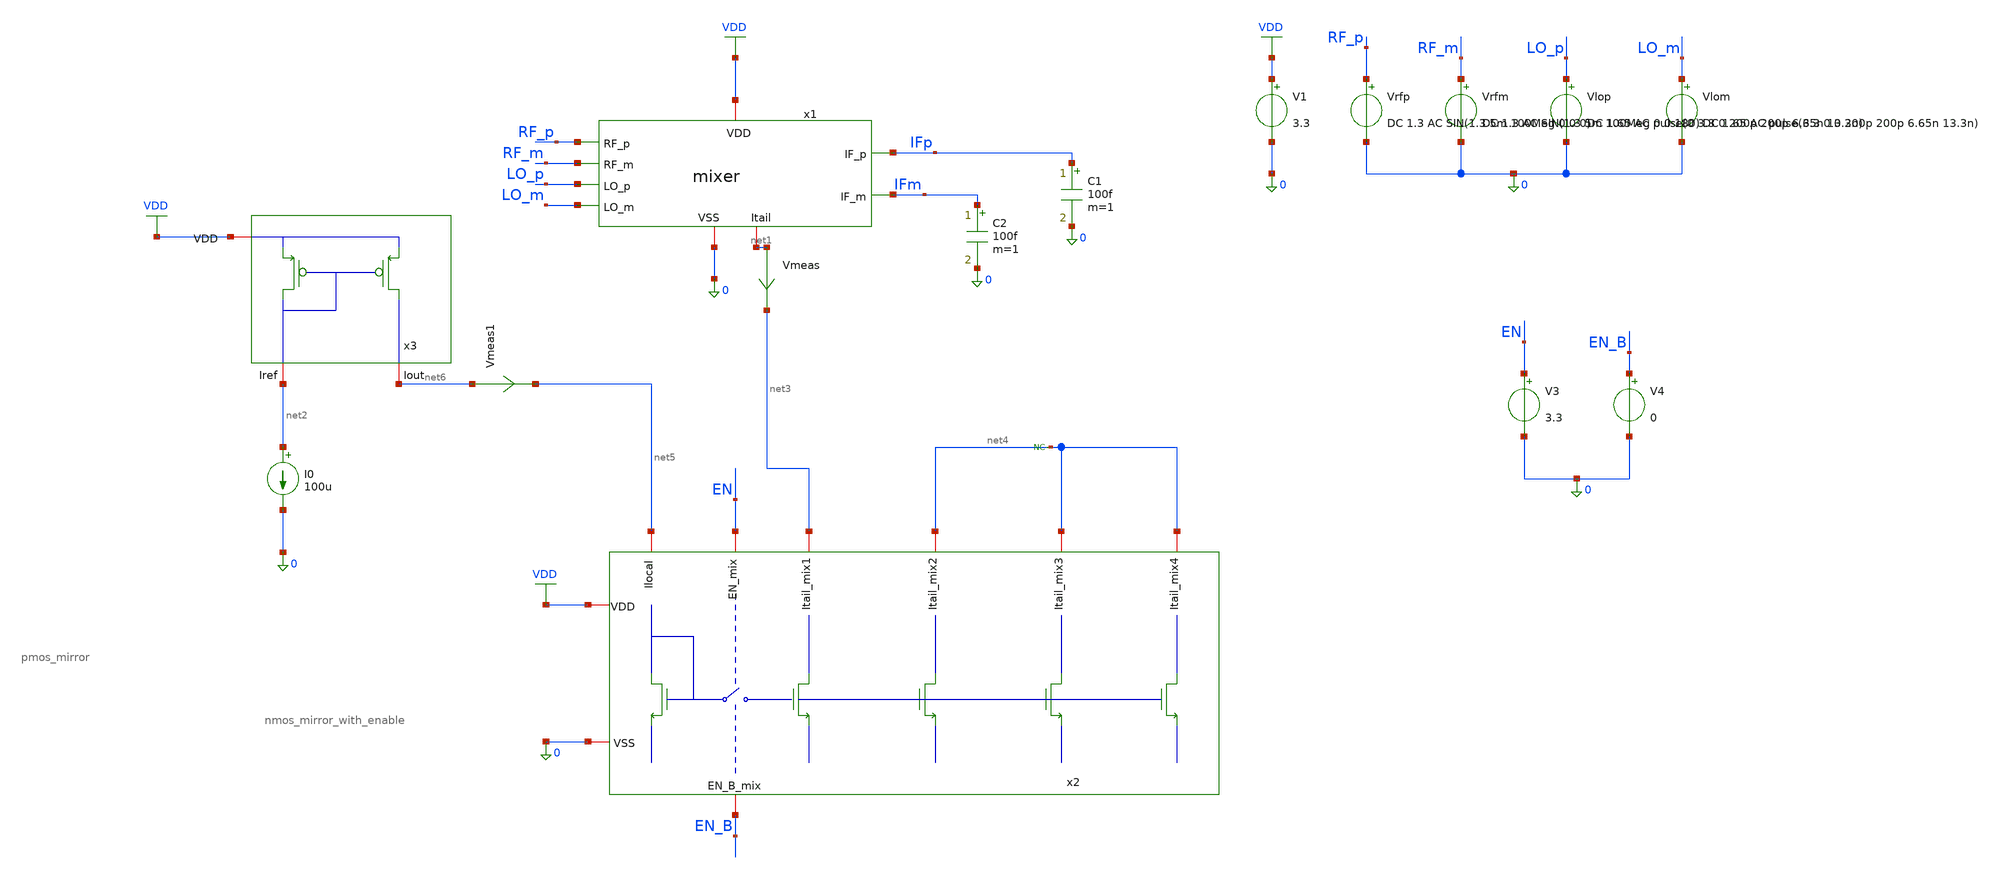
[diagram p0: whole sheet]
** sch_path: designs/mixer/testbench/mixer_with_mirror_tb.sch
**.subckt mixer_with_mirror_tb
V1 VDD 0 3.3
Vrfp RF_p 0 DC 1.3 AC SIN(1.3 5m 100Meg 0 0 0)
Vrfm RF_m 0 DC 1.3 AC SIN(1.3 5m 100Meg 0 0 180)
Vlop LO_p 0 DC 1.65 AC pulse(0 3.3 0 200p 200p 6.65n 13.3n)
Vlom LO_m 0 DC 1.65 AC pulse(3.3 0 0 200p 200p 6.65n 13.3n)
C1 IFp 0 100f m=1
C2 IFm 0 100f m=1
x1 IFp RF_p VDD 0 IFm RF_m LO_p net1 LO_m mixer
Vmeas net1 net3 0
.save i(vmeas)
x2 net4 net4 net5 VDD EN net3 0 EN_B net4 nmos_mirror_with_enable
x3 VDD net6 net2 pmos_mirror
I0 net2 0 100u
* noconn #net4
V3 EN 0 3.3
V4 EN_B 0 0
Vmeas1 net6 net5 0
.save i(vmeas1)
**** begin user architecture code

.include $::180MCU_MODELS/design.ngspice
.lib $::180MCU_MODELS/sm141064.ngspice typical
.lib $::180MCU_MODELS/sm141064.ngspice res_typical
* .lib $::180MCU_MODELS/sm141064.ngspice res_statistical




.control

destroy all
save all
write mixer_tb.raw

op
echo RF pair
print @m.x1.xm1.m0[gm]
print @m.x1.xm1.m0[id]
print @m.x1.xm1.m0[vgs]
print @m.x1.xm1.m0[vds]
print @m.x1.xm1.m0[vdsat]

echo LO pair
print @m.x1.xm3.m0[gm]
print @m.x1.xm3.m0[id]
print @m.x1.xm3.m0[vgs]
print @m.x1.xm3.m0[vds]
print @m.x1.xm3.m0[vdsat]

echo nmos tail
print @m.x2.xm6.m0[gm]
print @m.x2.xm6.m0[id]
print @m.x2.xm6.m0[vgs]
print @m.x2.xm6.m0[vds]
print @m.x2.xm6.m0[vdsat]

print i(vmeas)
print i(vmeas1)
print v(ifp) v(ifm)


;tran 0.01n 2u ;transient sim
let vrf = V(RF_p)-V(RF_m)
let vif = V(IFp)-V(IFm)

plot V(LO_p)
plot vrf
plot vif

fft vif vrf

plot mag(vif) vs frequency xlimit 0 500Meg
.endc


**** end user architecture code
**.ends
.GLOBAL VDD
.end
